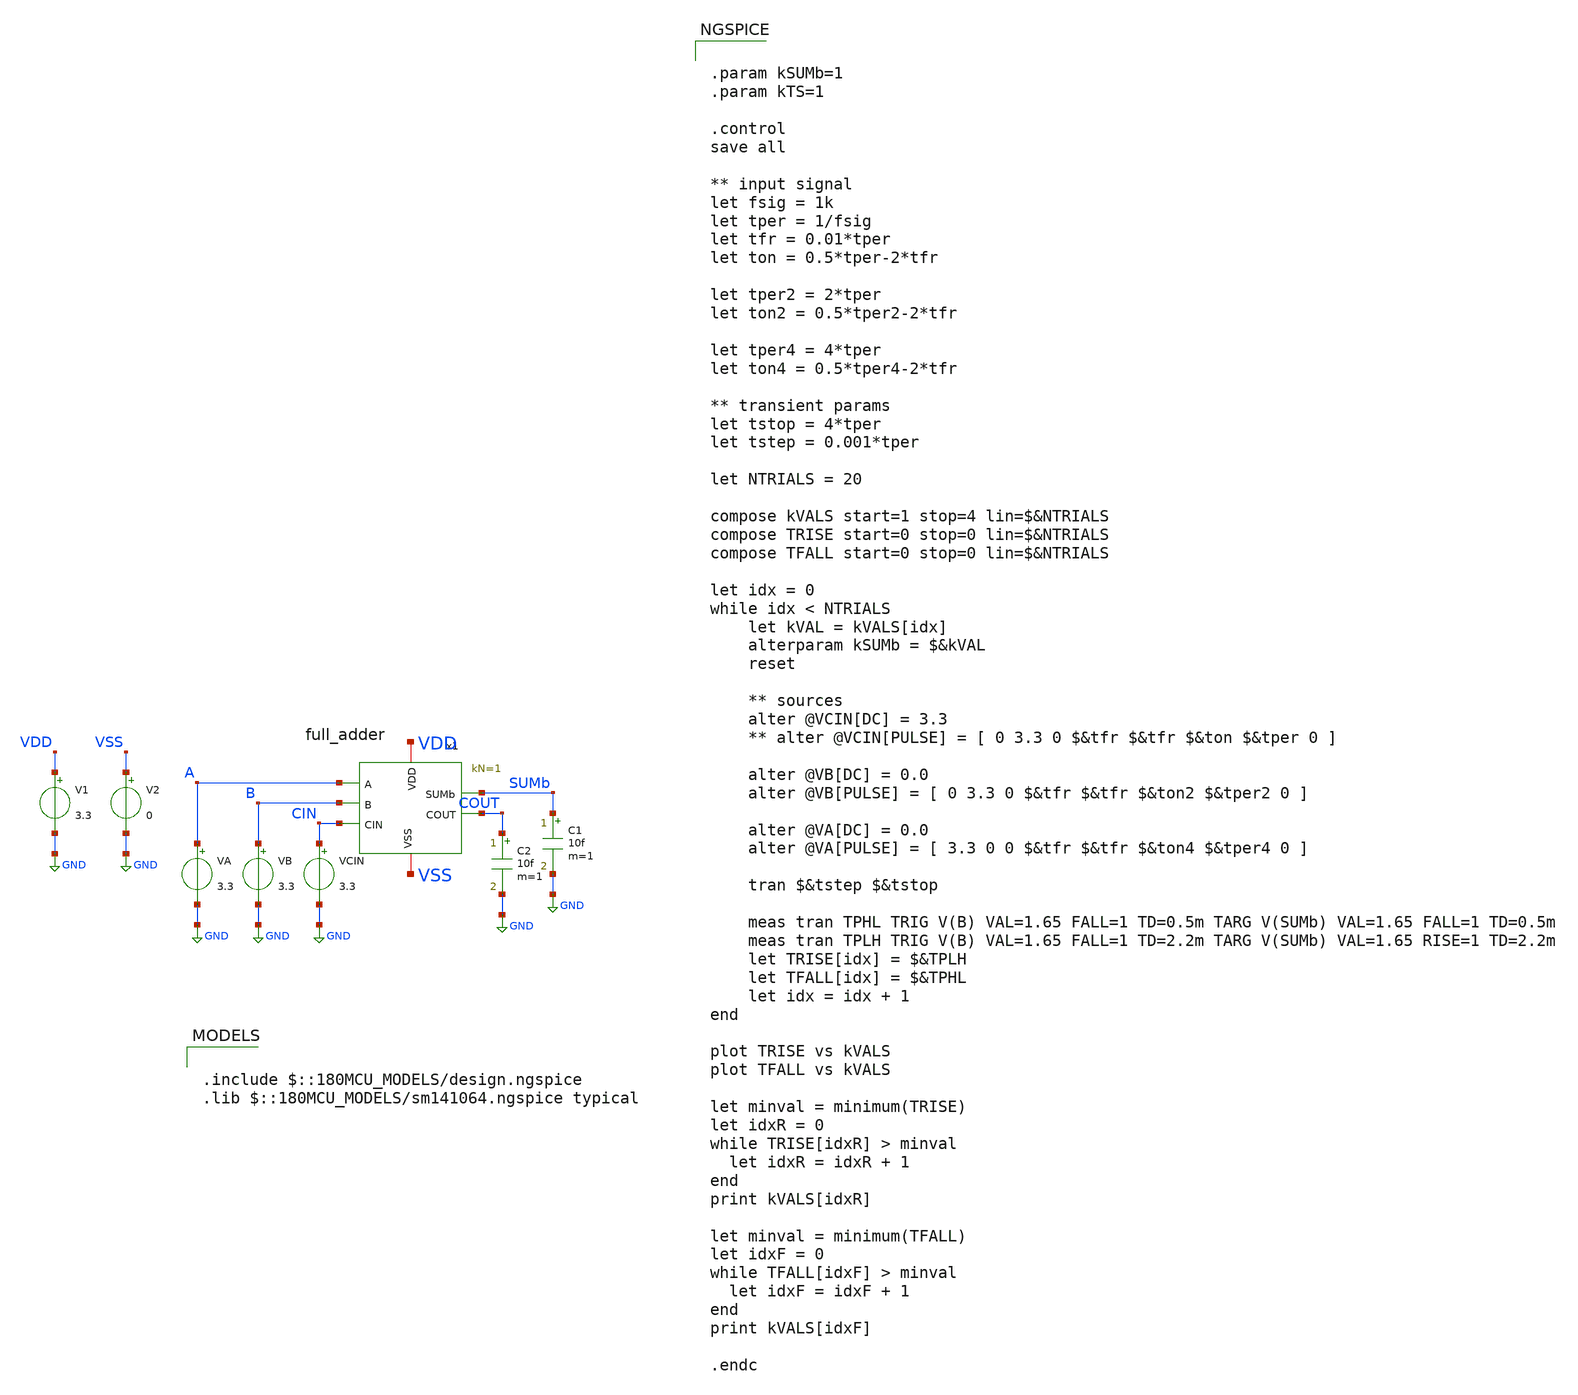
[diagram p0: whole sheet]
** sch_path: CAD4/full_adder_sizing_tb.sch
**.subckt full_adder_sizing_tb
V1 VDD GND 3.3
VA A GND 3.3
VB B GND 3.3
VCIN CIN GND 3.3
C1 SUMb GND 10f m=1
V2 VSS GND 0
x1 VDD VSS A B CIN SUMb COUT full_adder kN=1 kM=1
C2 COUT GND 10f m=1
**** begin user architecture code

.include $::180MCU_MODELS/design.ngspice
.lib $::180MCU_MODELS/sm141064.ngspice typical



.param kSUMb=1
.param kTS=1

.control
save all

** input signal
let fsig = 1k
let tper = 1/fsig
let tfr = 0.01*tper
let ton = 0.5*tper-2*tfr

let tper2 = 2*tper
let ton2 = 0.5*tper2-2*tfr

let tper4 = 4*tper
let ton4 = 0.5*tper4-2*tfr

** transient params
let tstop = 4*tper
let tstep = 0.001*tper

let NTRIALS = 20

compose kVALS start=1 stop=4 lin=$&NTRIALS
compose TRISE start=0 stop=0 lin=$&NTRIALS
compose TFALL start=0 stop=0 lin=$&NTRIALS

let idx = 0
while idx < NTRIALS
	let kVAL = kVALS[idx]
	alterparam kSUMb = $&kVAL
	reset

	** sources
	alter @VCIN[DC] = 3.3
	** alter @VCIN[PULSE] = [ 0 3.3 0 $&tfr $&tfr $&ton $&tper 0 ]

	alter @VB[DC] = 0.0
	alter @VB[PULSE] = [ 0 3.3 0 $&tfr $&tfr $&ton2 $&tper2 0 ]

	alter @VA[DC] = 0.0
	alter @VA[PULSE] = [ 3.3 0 0 $&tfr $&tfr $&ton4 $&tper4 0 ]

	tran $&tstep $&tstop

	meas tran TPHL TRIG V(B) VAL=1.65 FALL=1 TD=0.5m TARG V(SUMb) VAL=1.65 FALL=1 TD=0.5m
	meas tran TPLH TRIG V(B) VAL=1.65 FALL=1 TD=2.2m TARG V(SUMb) VAL=1.65 RISE=1 TD=2.2m
	let TRISE[idx] = $&TPLH
	let TFALL[idx] = $&TPHL
	let idx = idx + 1
end

plot TRISE vs kVALS
plot TFALL vs kVALS

let minval = minimum(TRISE)
let idxR = 0
while TRISE[idxR] > minval
  let idxR = idxR + 1
end
print kVALS[idxR]

let minval = minimum(TFALL)
let idxF = 0
while TFALL[idxF] > minval
  let idxF = idxF + 1
end
print kVALS[idxF]

.endc


**** end user architecture code
**.ends

* expanding   symbol:  engn1600-team1/CAD4/full_adder.sym # of pins=7
** sym_path: CAD4/full_adder.sym
** sch_path: CAD4/full_adder.sch
.subckt full_adder VDD VSS A B CIN SUMb COUT  kN=1 kM=1
*.iopin VDD
*.iopin VSS
*.ipin A
*.ipin B
*.ipin CIN
*.opin SUMb
*.opin COUT
XM1 net1 B VDD VDD pfet_03v3 L=0.28u W=0.72u nf=1 ad='int((nf+1)/2) * W/nf * 0.18u' as='int((nf+2)/2) * W/nf * 0.18u'
+ pd='2*int((nf+1)/2) * (W/nf + 0.18u)' ps='2*int((nf+2)/2) * (W/nf + 0.18u)' nrd='0.18u / W' nrs='0.18u / W'
+ sa=0 sb=0 sd=0 m=1
XM2 net4 A net1 VDD pfet_03v3 L=0.28u W=0.72u nf=1 ad='int((nf+1)/2) * W/nf * 0.18u' as='int((nf+2)/2) * W/nf * 0.18u'
+ pd='2*int((nf+1)/2) * (W/nf + 0.18u)' ps='2*int((nf+2)/2) * (W/nf + 0.18u)' nrd='0.18u / W' nrs='0.18u / W'
+ sa=0 sb=0 sd=0 m=1
XM3 net3 A VDD VDD pfet_03v3 L=0.28u W=0.72u nf=1 ad='int((nf+1)/2) * W/nf * 0.18u' as='int((nf+2)/2) * W/nf * 0.18u'
+ pd='2*int((nf+1)/2) * (W/nf + 0.18u)' ps='2*int((nf+2)/2) * (W/nf + 0.18u)' nrd='0.18u / W' nrs='0.18u / W'
+ sa=0 sb=0 sd=0 m=1
XM4 net3 B VDD VDD pfet_03v3 L=0.28u W=0.72u nf=1 ad='int((nf+1)/2) * W/nf * 0.18u' as='int((nf+2)/2) * W/nf * 0.18u'
+ pd='2*int((nf+1)/2) * (W/nf + 0.18u)' ps='2*int((nf+2)/2) * (W/nf + 0.18u)' nrd='0.18u / W' nrs='0.18u / W'
+ sa=0 sb=0 sd=0 m=1
XM5 net4 CIN net3 VDD pfet_03v3 L=0.28u W=0.72u nf=1 ad='int((nf+1)/2) * W/nf * 0.18u' as='int((nf+2)/2) * W/nf * 0.18u'
+ pd='2*int((nf+1)/2) * (W/nf + 0.18u)' ps='2*int((nf+2)/2) * (W/nf + 0.18u)' nrd='0.18u / W' nrs='0.18u / W'
+ sa=0 sb=0 sd=0 m=1
XM6 net4 CIN net5 VSS nfet_03v3 L=0.28u W=0.36u nf=1 ad='int((nf+1)/2) * W/nf * 0.18u' as='int((nf+2)/2) * W/nf * 0.18u'
+ pd='2*int((nf+1)/2) * (W/nf + 0.18u)' ps='2*int((nf+2)/2) * (W/nf + 0.18u)' nrd='0.18u / W' nrs='0.18u / W'
+ sa=0 sb=0 sd=0 m=1
XM7 net2 B VSS VSS nfet_03v3 L=0.28u W=0.36u nf=1 ad='int((nf+1)/2) * W/nf * 0.18u' as='int((nf+2)/2) * W/nf * 0.18u'
+ pd='2*int((nf+1)/2) * (W/nf + 0.18u)' ps='2*int((nf+2)/2) * (W/nf + 0.18u)' nrd='0.18u / W' nrs='0.18u / W'
+ sa=0 sb=0 sd=0 m=1
XM8 net4 A net2 VSS nfet_03v3 L=0.28u W=0.36u nf=1 ad='int((nf+1)/2) * W/nf * 0.18u' as='int((nf+2)/2) * W/nf * 0.18u'
+ pd='2*int((nf+1)/2) * (W/nf + 0.18u)' ps='2*int((nf+2)/2) * (W/nf + 0.18u)' nrd='0.18u / W' nrs='0.18u / W'
+ sa=0 sb=0 sd=0 m=1
XM9 net5 A VSS VSS nfet_03v3 L=0.28u W=0.36u nf=1 ad='int((nf+1)/2) * W/nf * 0.18u' as='int((nf+2)/2) * W/nf * 0.18u'
+ pd='2*int((nf+1)/2) * (W/nf + 0.18u)' ps='2*int((nf+2)/2) * (W/nf + 0.18u)' nrd='0.18u / W' nrs='0.18u / W'
+ sa=0 sb=0 sd=0 m=1
XM10 net5 B VSS VSS nfet_03v3 L=0.28u W=0.36u nf=1 ad='int((nf+1)/2) * W/nf * 0.18u' as='int((nf+2)/2) * W/nf * 0.18u'
+ pd='2*int((nf+1)/2) * (W/nf + 0.18u)' ps='2*int((nf+2)/2) * (W/nf + 0.18u)' nrd='0.18u / W' nrs='0.18u / W'
+ sa=0 sb=0 sd=0 m=1
XM11 SUMb net4 net7 VDD pfet_03v3 L=0.28u W='kSUMb*0.72u' nf=1 ad='int((nf+1)/2) * W/nf * 0.18u' as='int((nf+2)/2) * W/nf * 0.18u'
+ pd='2*int((nf+1)/2) * (W/nf + 0.18u)' ps='2*int((nf+2)/2) * (W/nf + 0.18u)' nrd='0.18u / W' nrs='0.18u / W'
+ sa=0 sb=0 sd=0 m=1
XM12 net7 A VDD VDD pfet_03v3 L=0.28u W=0.72u nf=1 ad='int((nf+1)/2) * W/nf * 0.18u' as='int((nf+2)/2) * W/nf * 0.18u'
+ pd='2*int((nf+1)/2) * (W/nf + 0.18u)' ps='2*int((nf+2)/2) * (W/nf + 0.18u)' nrd='0.18u / W' nrs='0.18u / W'
+ sa=0 sb=0 sd=0 m=1
XM13 net7 CIN VDD VDD pfet_03v3 L=0.28u W=0.72u nf=1 ad='int((nf+1)/2) * W/nf * 0.18u' as='int((nf+2)/2) * W/nf * 0.18u'
+ pd='2*int((nf+1)/2) * (W/nf + 0.18u)' ps='2*int((nf+2)/2) * (W/nf + 0.18u)' nrd='0.18u / W' nrs='0.18u / W'
+ sa=0 sb=0 sd=0 m=1
XM14 net7 B VDD VDD pfet_03v3 L=0.28u W=0.72u nf=1 ad='int((nf+1)/2) * W/nf * 0.18u' as='int((nf+2)/2) * W/nf * 0.18u'
+ pd='2*int((nf+1)/2) * (W/nf + 0.18u)' ps='2*int((nf+2)/2) * (W/nf + 0.18u)' nrd='0.18u / W' nrs='0.18u / W'
+ sa=0 sb=0 sd=0 m=1
XM15 net8 A net9 VDD pfet_03v3 L=0.28u W=0.72u nf=1 ad='int((nf+1)/2) * W/nf * 0.18u' as='int((nf+2)/2) * W/nf * 0.18u'
+ pd='2*int((nf+1)/2) * (W/nf + 0.18u)' ps='2*int((nf+2)/2) * (W/nf + 0.18u)' nrd='0.18u / W' nrs='0.18u / W'
+ sa=0 sb=0 sd=0 m=1
XM16 SUMb CIN net8 VDD pfet_03v3 L=0.28u W='kTS*0.72u' nf=1 ad='int((nf+1)/2) * W/nf * 0.18u' as='int((nf+2)/2) * W/nf * 0.18u'
+ pd='2*int((nf+1)/2) * (W/nf + 0.18u)' ps='2*int((nf+2)/2) * (W/nf + 0.18u)' nrd='0.18u / W' nrs='0.18u / W'
+ sa=0 sb=0 sd=0 m=1
XM17 net9 B VDD VDD pfet_03v3 L=0.28u W=0.72u nf=1 ad='int((nf+1)/2) * W/nf * 0.18u' as='int((nf+2)/2) * W/nf * 0.18u'
+ pd='2*int((nf+1)/2) * (W/nf + 0.18u)' ps='2*int((nf+2)/2) * (W/nf + 0.18u)' nrd='0.18u / W' nrs='0.18u / W'
+ sa=0 sb=0 sd=0 m=1
XM18 SUMb net4 net6 VSS nfet_03v3 L=0.28u W='kSUMb*0.36u' nf=1 ad='int((nf+1)/2) * W/nf * 0.18u' as='int((nf+2)/2) * W/nf * 0.18u'
+ pd='2*int((nf+1)/2) * (W/nf + 0.18u)' ps='2*int((nf+2)/2) * (W/nf + 0.18u)' nrd='0.18u / W' nrs='0.18u / W'
+ sa=0 sb=0 sd=0 m=1
XM19 net6 B VSS VSS nfet_03v3 L=0.28u W=0.36u nf=1 ad='int((nf+1)/2) * W/nf * 0.18u' as='int((nf+2)/2) * W/nf * 0.18u'
+ pd='2*int((nf+1)/2) * (W/nf + 0.18u)' ps='2*int((nf+2)/2) * (W/nf + 0.18u)' nrd='0.18u / W' nrs='0.18u / W'
+ sa=0 sb=0 sd=0 m=1
XM20 net6 A VSS VSS nfet_03v3 L=0.28u W=0.36u nf=1 ad='int((nf+1)/2) * W/nf * 0.18u' as='int((nf+2)/2) * W/nf * 0.18u'
+ pd='2*int((nf+1)/2) * (W/nf + 0.18u)' ps='2*int((nf+2)/2) * (W/nf + 0.18u)' nrd='0.18u / W' nrs='0.18u / W'
+ sa=0 sb=0 sd=0 m=1
XM21 net6 CIN VSS VSS nfet_03v3 L=0.28u W=0.36u nf=1 ad='int((nf+1)/2) * W/nf * 0.18u' as='int((nf+2)/2) * W/nf * 0.18u'
+ pd='2*int((nf+1)/2) * (W/nf + 0.18u)' ps='2*int((nf+2)/2) * (W/nf + 0.18u)' nrd='0.18u / W' nrs='0.18u / W'
+ sa=0 sb=0 sd=0 m=1
XM22 SUMb CIN net11 VSS nfet_03v3 L=0.28u W='kTS*0.36u' nf=1 ad='int((nf+1)/2) * W/nf * 0.18u' as='int((nf+2)/2) * W/nf * 0.18u'
+ pd='2*int((nf+1)/2) * (W/nf + 0.18u)' ps='2*int((nf+2)/2) * (W/nf + 0.18u)' nrd='0.18u / W' nrs='0.18u / W'
+ sa=0 sb=0 sd=0 m=1
XM23 net11 A net10 VSS nfet_03v3 L=0.28u W=0.36u nf=1 ad='int((nf+1)/2) * W/nf * 0.18u' as='int((nf+2)/2) * W/nf * 0.18u'
+ pd='2*int((nf+1)/2) * (W/nf + 0.18u)' ps='2*int((nf+2)/2) * (W/nf + 0.18u)' nrd='0.18u / W' nrs='0.18u / W'
+ sa=0 sb=0 sd=0 m=1
XM24 net10 B VSS VSS nfet_03v3 L=0.28u W=0.36u nf=1 ad='int((nf+1)/2) * W/nf * 0.18u' as='int((nf+2)/2) * W/nf * 0.18u'
+ pd='2*int((nf+1)/2) * (W/nf + 0.18u)' ps='2*int((nf+2)/2) * (W/nf + 0.18u)' nrd='0.18u / W' nrs='0.18u / W'
+ sa=0 sb=0 sd=0 m=1
XM25 COUT net4 VDD VDD pfet_03v3 L=0.28u W=0.72u nf=1 ad='int((nf+1)/2) * W/nf * 0.18u' as='int((nf+2)/2) * W/nf * 0.18u'
+ pd='2*int((nf+1)/2) * (W/nf + 0.18u)' ps='2*int((nf+2)/2) * (W/nf + 0.18u)' nrd='0.18u / W' nrs='0.18u / W'
+ sa=0 sb=0 sd=0 m=1
XM26 COUT net4 VSS VSS nfet_03v3 L=0.28u W=0.36u nf=1 ad='int((nf+1)/2) * W/nf * 0.18u' as='int((nf+2)/2) * W/nf * 0.18u'
+ pd='2*int((nf+1)/2) * (W/nf + 0.18u)' ps='2*int((nf+2)/2) * (W/nf + 0.18u)' nrd='0.18u / W' nrs='0.18u / W'
+ sa=0 sb=0 sd=0 m=1
**** begin user architecture code


.param kSUMb=1
.param kTS=1


**** end user architecture code
.ends

.GLOBAL GND
.end
